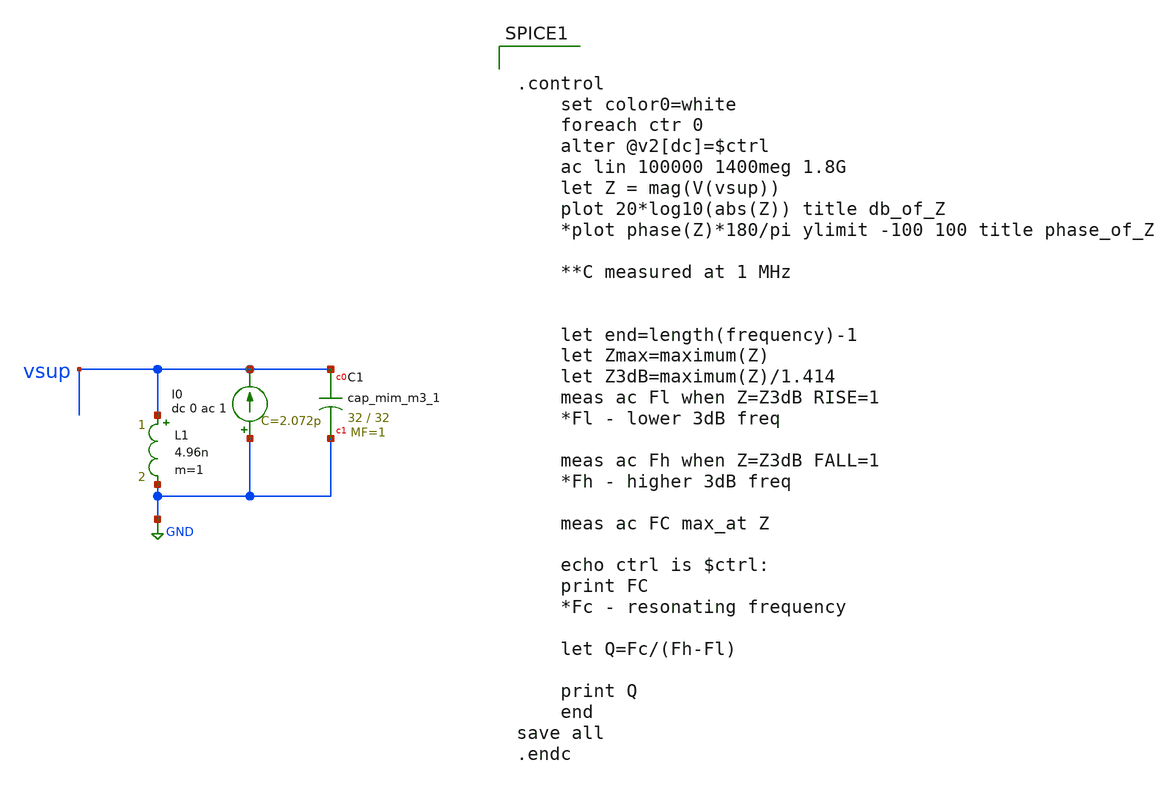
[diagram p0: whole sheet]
** sch_path: cap_meas/capmeas.sch
**.subckt capmeas
I0 GND vsup dc 0 ac 1
L1 vsup GND 4.96n m=1
XC1 vsup GND sky130_fd_pr__cap_mim_m3_1 W=32 L=32 MF=1 m=1
**** begin user architecture code


.option wnflag = 1
.lib /usr/local/share/pdk/sky130A/libs.tech/ngspice/sky130.lib.spice tt
.include /usr/local/share/pdk/sky130A/libs.ref/sky130_fd_pr/spice/sky130_fd_pr__ind_05_220.model.spice
.param mc_mm_switch=0




.control
	set color0=white
	foreach ctr 0
	alter @v2[dc]=$ctrl
	ac lin 100000 1400meg 1.8G
	let Z = mag(V(vsup))
	plot 20*log10(abs(Z)) title db_of_Z
	*plot phase(Z)*180/pi ylimit -100 100 title phase_of_Z

	**C measured at 1 MHz


	let end=length(frequency)-1
	let Zmax=maximum(Z)
	let Z3dB=maximum(Z)/1.414
	meas ac Fl when Z=Z3dB RISE=1
	*Fl - lower 3dB freq

	meas ac Fh when Z=Z3dB FALL=1
	*Fh - higher 3dB freq

	meas ac FC max_at Z

	echo ctrl is $ctrl:
	print FC
	*Fc - resonating frequency

	let Q=Fc/(Fh-Fl)

	print Q
	end
save all
.endc


**** end user architecture code
**.ends
.GLOBAL GND
.end
